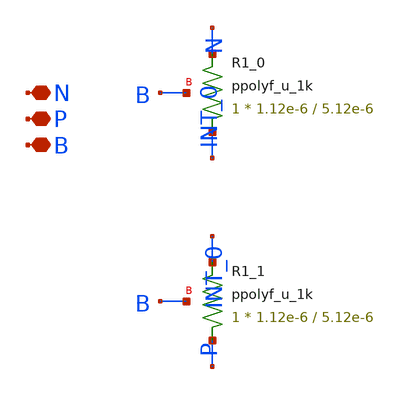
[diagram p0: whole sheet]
** sch_path: design/LELO_TR_GF180MCUD/LELOTR_RES2.sch
**.subckt LELOTR_RES2 N P B
*.iopin N
*.iopin P
*.iopin B
XR1_0 INT_0 N B ppolyf_u_1k r_width=1.12e-6 r_length=5.12e-6 m=1
XR1_1 P INT_0 B ppolyf_u_1k r_width=1.12e-6 r_length=5.12e-6 m=1
**.ends
.end
